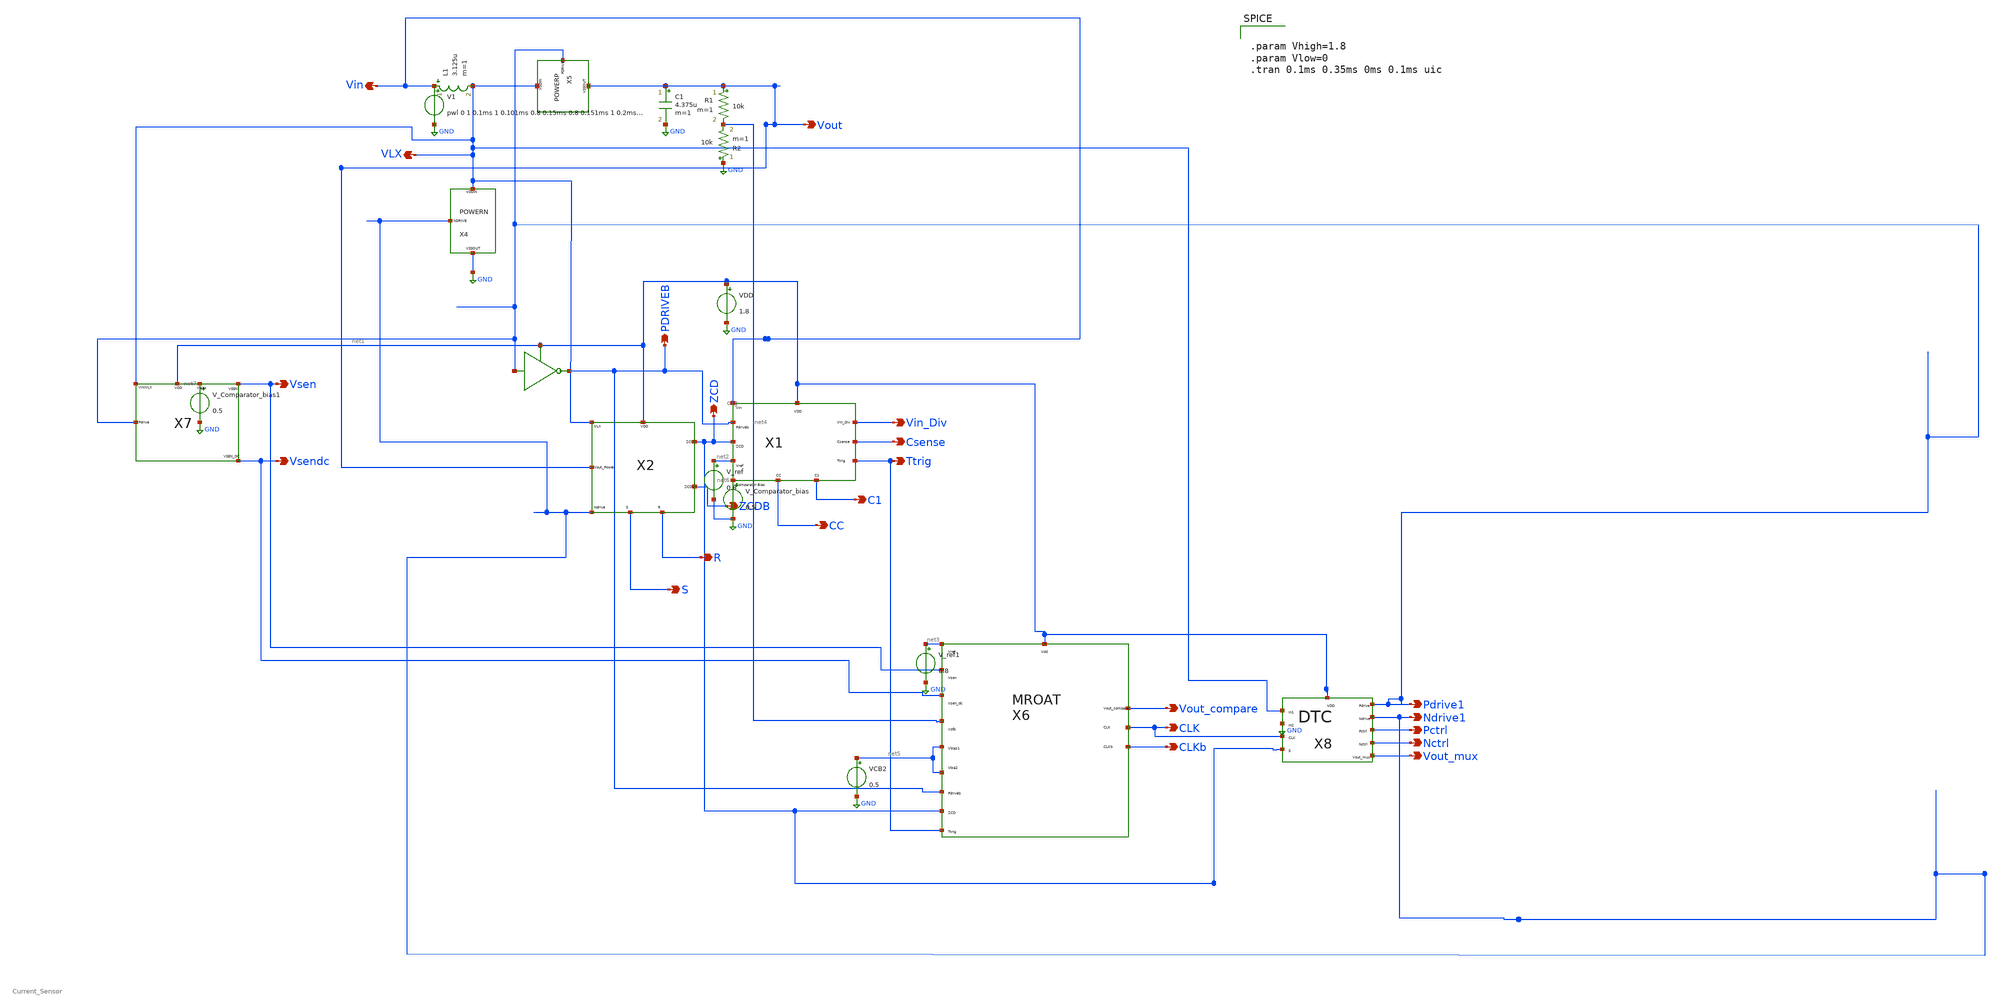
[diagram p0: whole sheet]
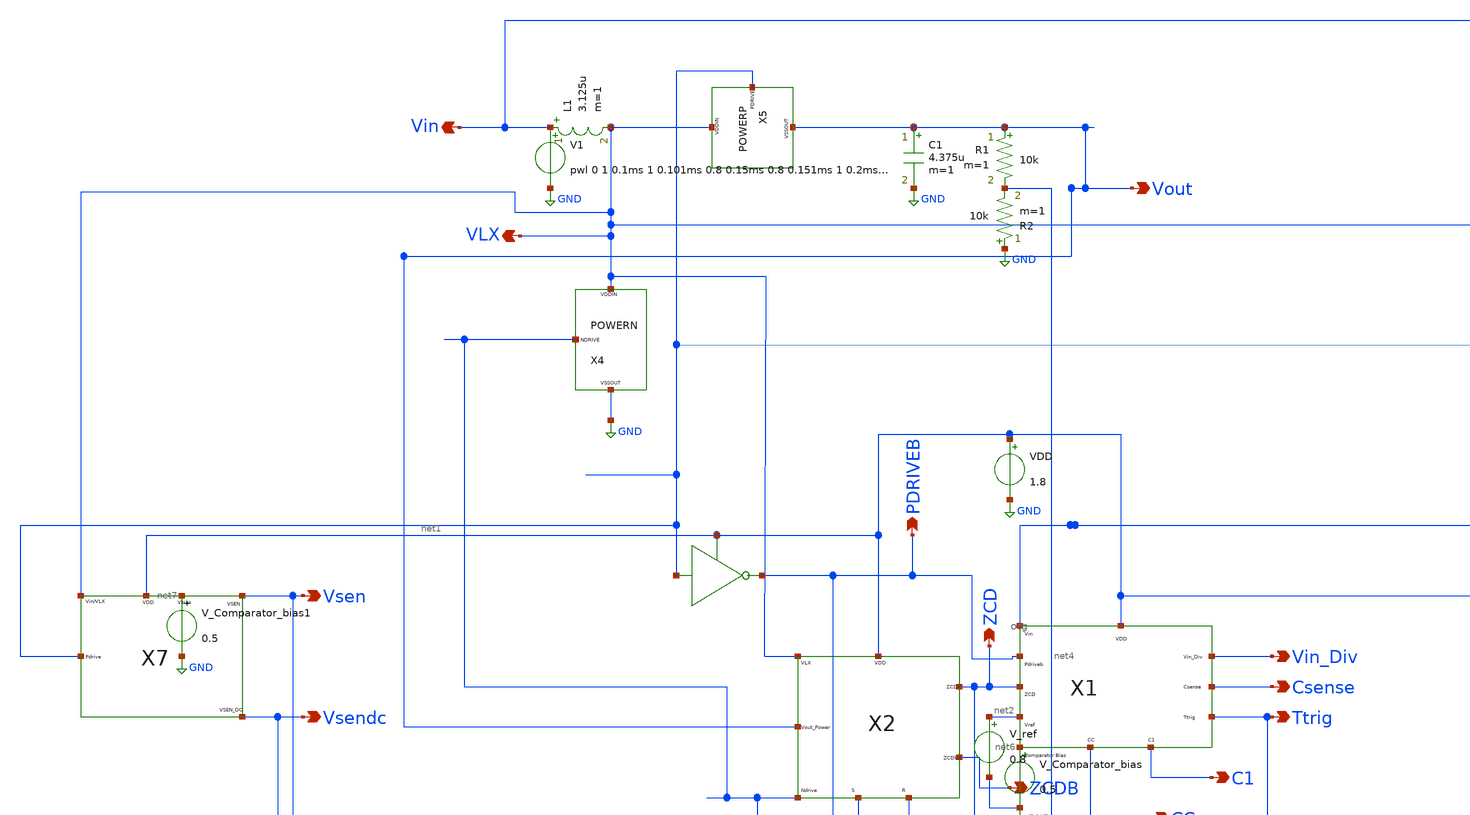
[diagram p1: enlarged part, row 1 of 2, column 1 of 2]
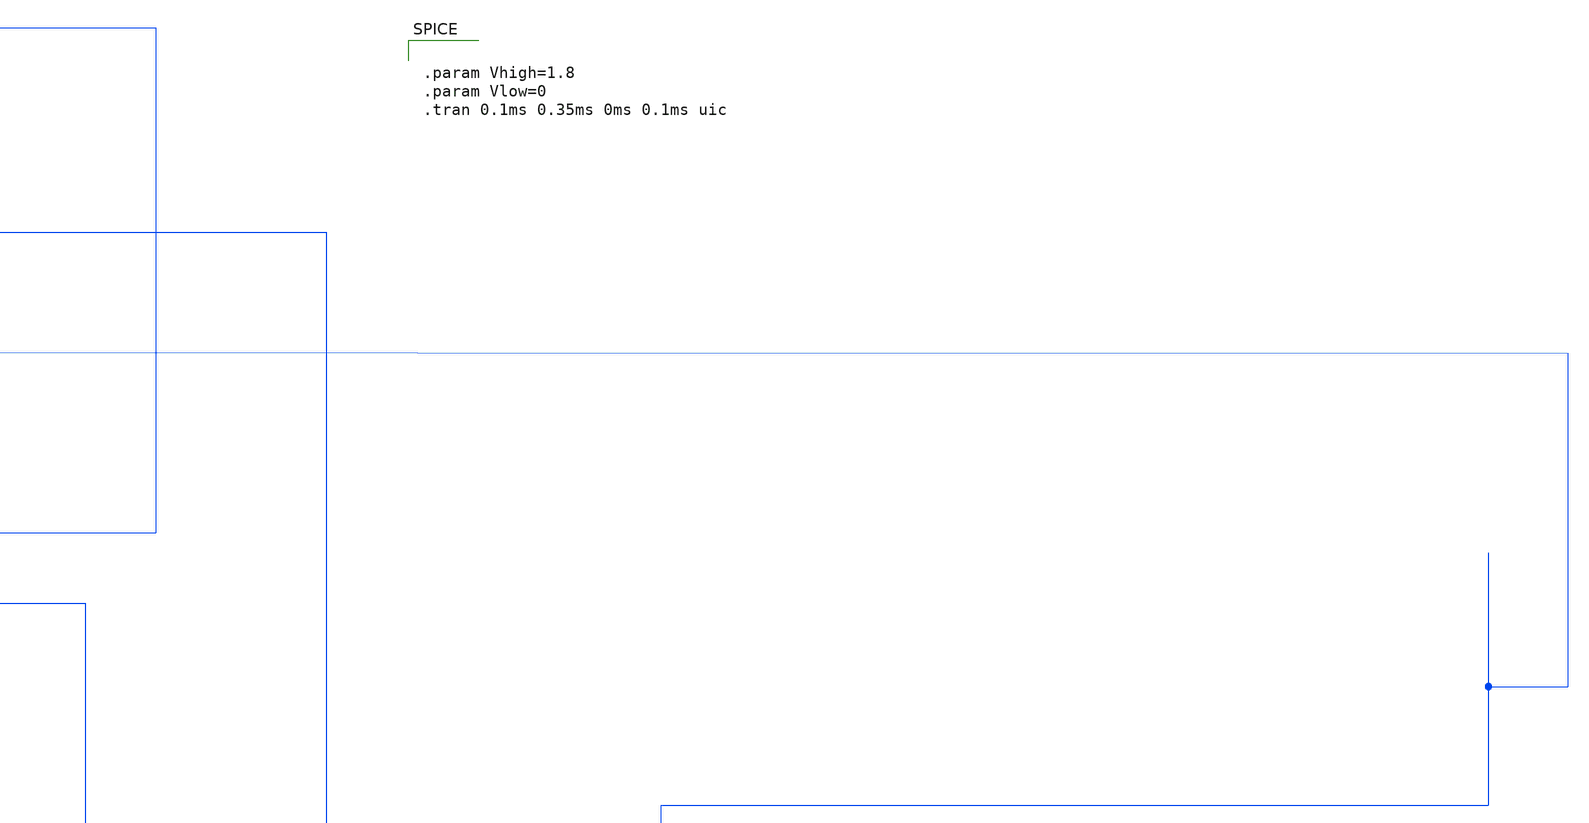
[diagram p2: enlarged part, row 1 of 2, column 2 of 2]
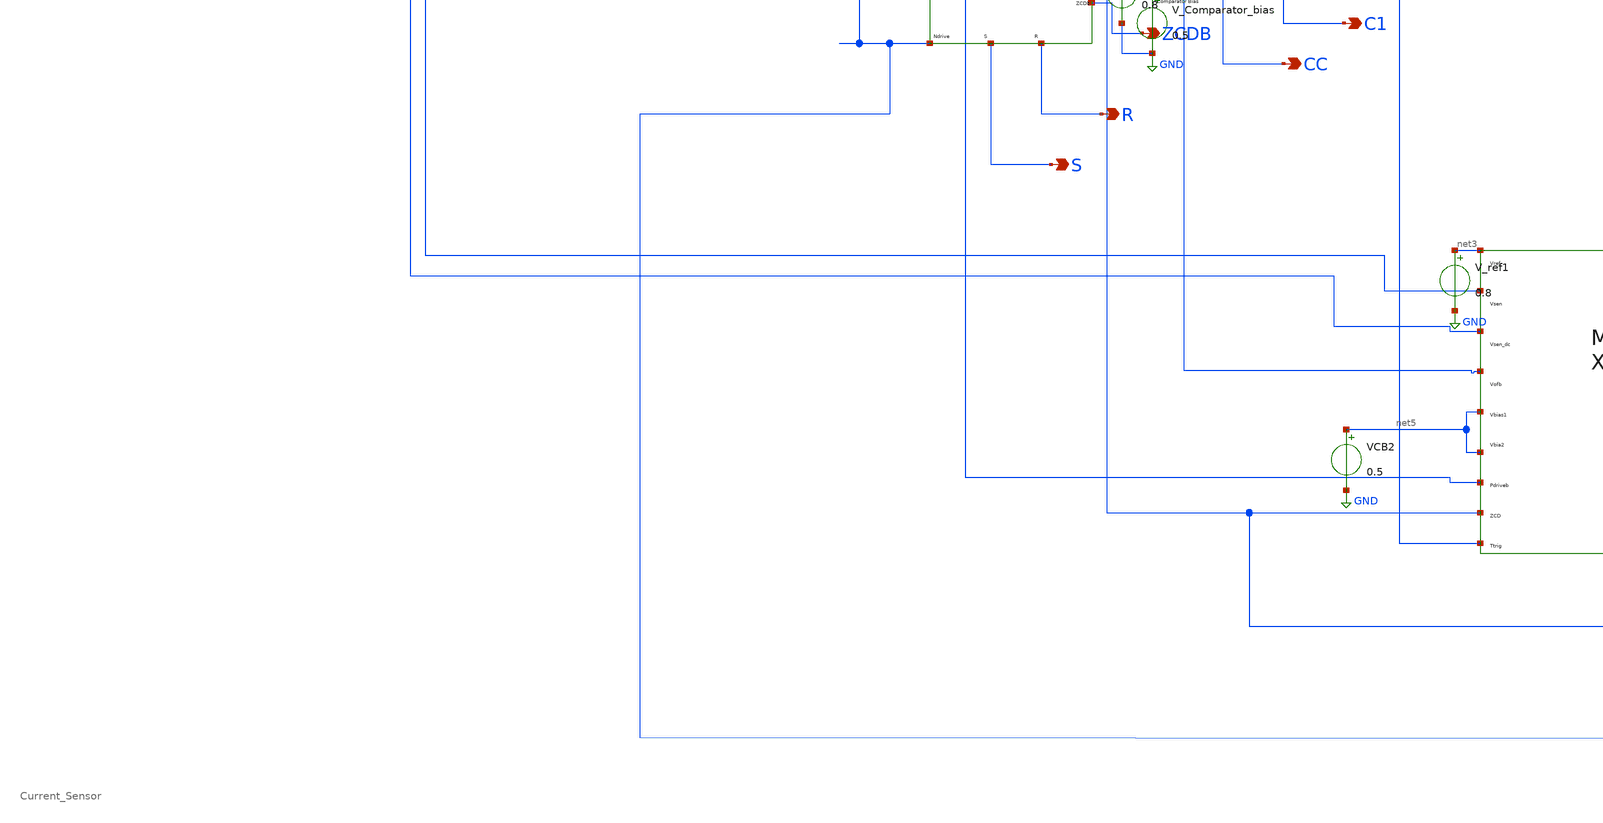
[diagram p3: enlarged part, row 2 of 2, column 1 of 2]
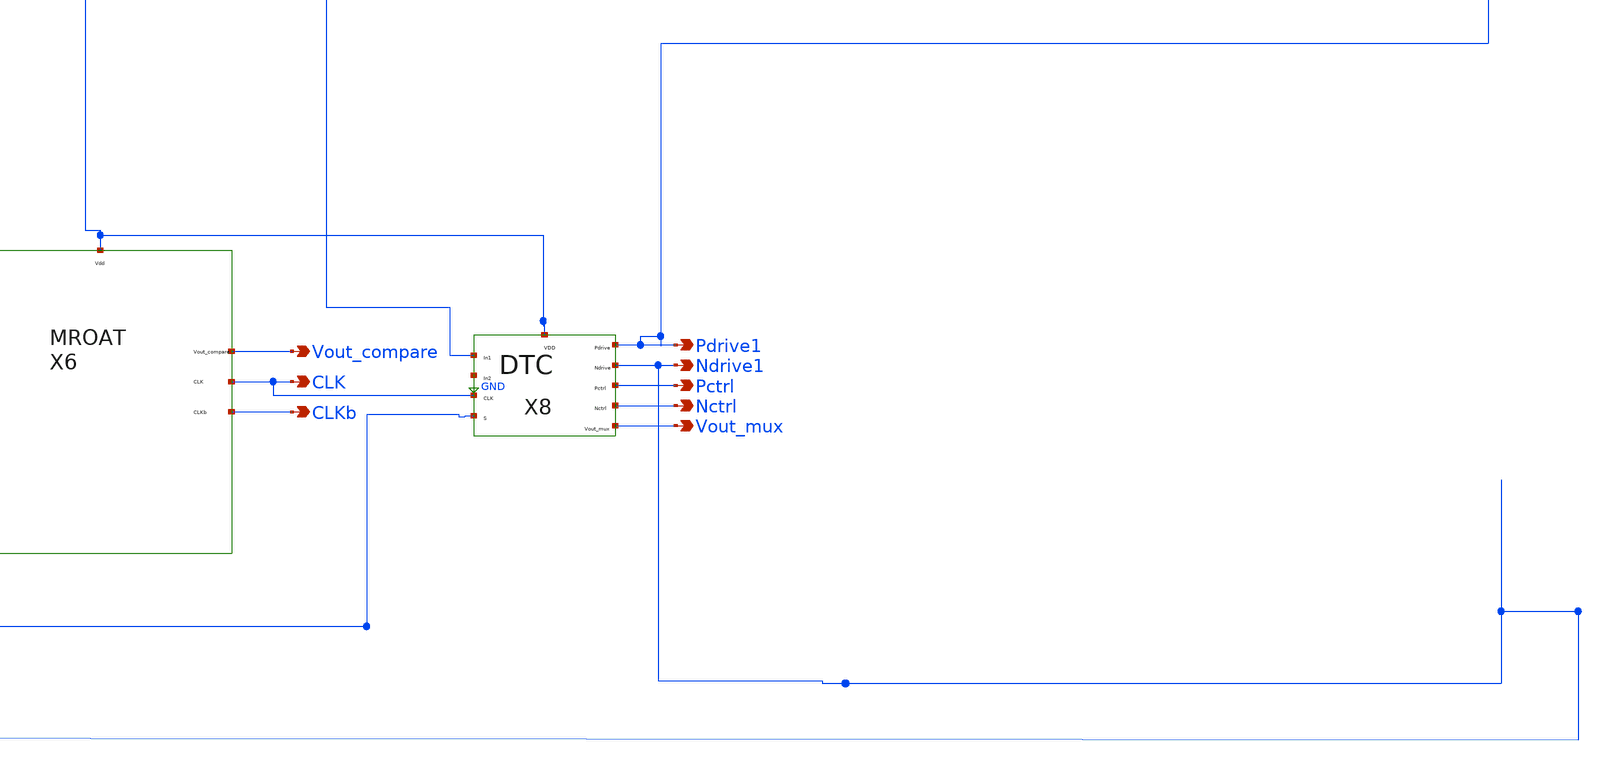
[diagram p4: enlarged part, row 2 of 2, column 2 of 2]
** sch_path: Current Sensor/fb_test.sch
**.subckt fb_test ZCD Vin_Div Csense Ttrig ZCDB PDRIVEB Vin VLX Vout C1 CC S R Vsen Vsendc
*+ Vout_compare CLK CLKb Pdrive1 Ndrive1 Pctrl Nctrl Vout_mux
*.opin ZCD
*.opin Vin_Div
*.opin Csense
*.opin Ttrig
*.opin ZCDB
*.opin PDRIVEB
*.opin Vin
*.opin VLX
*.opin Vout
*.opin C1
*.opin CC
*.opin S
*.opin R
*.opin Vsen
*.opin Vsendc
*.opin Vout_compare
*.opin CLK
*.opin CLKb
*.opin Pdrive1
*.opin Ndrive1
*.opin Pctrl
*.opin Nctrl
*.opin Vout_mux
X1 Vin PDRIVEB ZCD net2 net6 net1 Vin_Div Csense Ttrig CC C1 otg
X2 VLX Vout Ndrive1 net1 ZCD ZCDB S R zcd
VDD net1 GND 1.8
V_Comparator_bias net6 GND 0.5
V_ref net2 GND 0.8
C1 Vout GND 4.375u m=1
R1 Vout net4 10k m=1
L1 Vin VLX 3.125u m=1
X4 Ndrive1 VLX GND powern
X5 Pdrive1 VLX Vout powerp
R2 GND net4 10k m=1
X7 Vsen Vsendc Pdrive1 VLX net1 net7 Current_Sensor
V_Comparator_bias1 net7 GND 0.5
V1 Vin GND pwl 0 1 0.1ms 1 0.101ms 0.8 0.15ms 0.8 0.151ms 1 0.2ms 1 0.3ms 1 0.301ms 1.2 0.35ms 1.2
+ 0.351ms 1 0.4ms 1
X6 net3 Vsen Vsendc net4 net5 net5 net1 Vout_compare PDRIVEB ZCD Ttrig CLK CLKb mroat
V_ref1 net3 GND 0.8
VCB2 net5 GND 0.5
X8 net1 VLX GND CLK ZCD Pdrive1 Ndrive1 Pctrl Nctrl Vout_mux dtc
**** begin user architecture code

** opencircuitdesign pdks install
.lib $::SKYWATER_MODELS/sky130.lib.spice tt_mm




.param Vhigh=1.8
.param Vlow=0
.tran 0.1ms 0.35ms 0ms 0.1ms uic

**** end user architecture code
**.ends
.GLOBAL GND
.end
